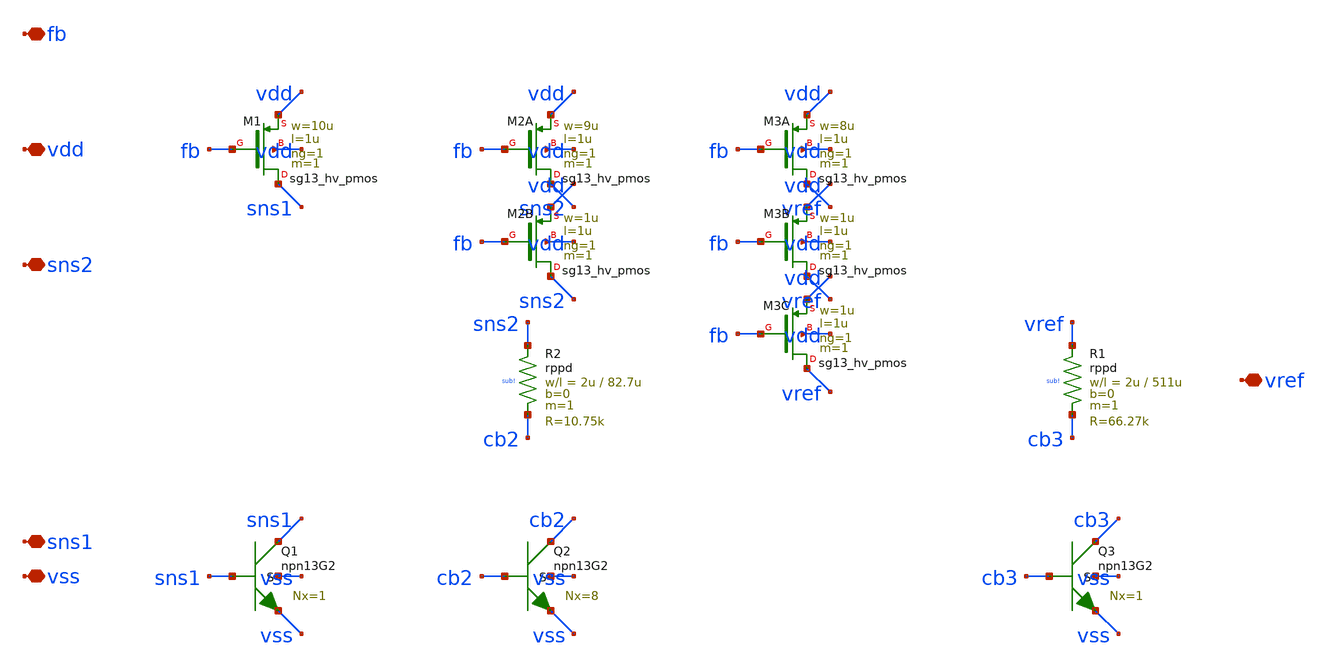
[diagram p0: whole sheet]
** sch_path: designs/g1-guardian/blocks/g1_bgr/source/2AMLogic-sg13g2-bandgap/bandgap_core.sch
**.subckt bandgap_core vdd vss fb sns1 sns2 vref
*.iopin vdd
*.iopin vss
*.iopin fb
*.iopin sns1
*.iopin sns2
*.iopin vref
XM1 sns1 fb vdd vdd sg13_hv_pmos w=10u l=1u ng=1 m=1 mm_ok=1
XQ1 sns1 sns1 vss vss npn13G2 Nx=1 mm_ok=1
XM2A sns2 fb vdd vdd sg13_hv_pmos w=9u l=1u ng=1 m=1 mm_ok=1
XM2B sns2 fb vdd vdd sg13_hv_pmos w=1u l=1u ng=1 m=1 mm_ok=1
XR2 sns2 cb2 sub! rppd w=2u l=82.7u m=1 b=0 mm_ok=1
XQ2 cb2 cb2 vss vss npn13G2 Nx=8 mm_ok=1
XM3A vref fb vdd vdd sg13_hv_pmos w=8u l=1u ng=1 m=1 mm_ok=1
XM3B vref fb vdd vdd sg13_hv_pmos w=1u l=1u ng=1 m=1 mm_ok=1
XM3C vref fb vdd vdd sg13_hv_pmos w=1u l=1u ng=1 m=1 mm_ok=1
XR1 vref cb3 sub! rppd w=2u l=511u m=1 b=0 mm_ok=1
XQ3 cb3 cb3 vss vss npn13G2 Nx=1 mm_ok=1
**.ends
.end
